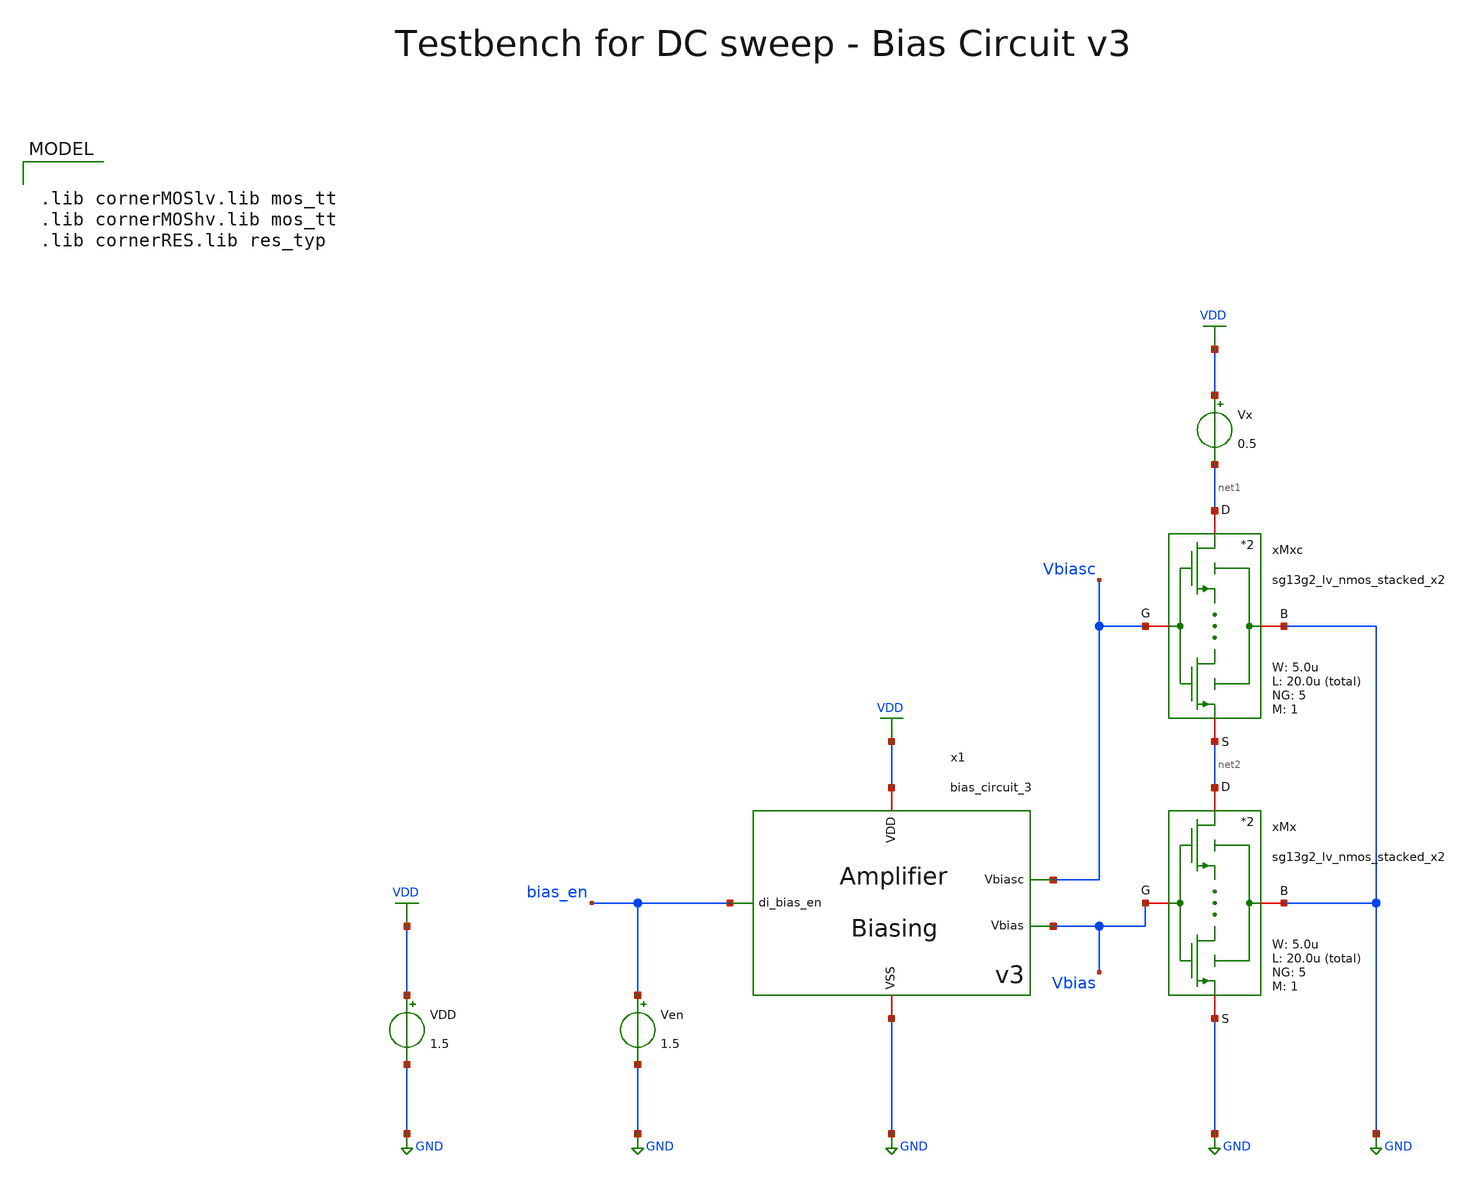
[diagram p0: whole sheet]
** sch_path: SG13G2_ATBS-ADC-main/xschem/bio_amplifier/amplifier_core/bias_circuit/bias_circuit_3/testbenches/bias_circuit_3_tb_dc.sch
**.subckt bias_circuit_3_tb_dc
Ven bias_en GND 1.5
VDD VDD GND 1.5
x1 bias_en VDD GND Vbias Vbiasc bias_circuit_3
Vx VDD net1 0.5
xMx net2 Vbias GND GND sg13g2_lv_nmos_stacked_x2 W_N=5.0u L_N=20.0u NG_N=5 M_N=1
xMxc net1 Vbiasc GND net2 sg13g2_lv_nmos_stacked_x2 W_N=5.0u L_N=20.0u NG_N=5 M_N=1
**** begin user architecture code

.lib cornerMOSlv.lib mos_tt
.lib cornerMOShv.lib mos_tt
.lib cornerRES.lib res_typ



.param temp=27
.options savecurrents method=gear reltol=1e-2 abstol=1e-15 gmin=1e-15
.control

save all

* Operating Point Analysis
op
remzerovec
write bias_circuit_3_tb_dc.raw
set appendwrite

* DC Sweep of Vout
dc Vx 0 1.5 5m
remzerovec
write bias_circuit_3_tb_dc.raw

* Plotting
plot i(Vx) xlabel Vx

* Measurements
meas dc Ix_1V FIND i(Vx) at=1
meas dc Ix_0V FIND i(Vx) at=0
let Ix_volt = Ix_0V - Ix_1V
print Ix_volt

* DC Sweep of VDD
dc VDD 0 1.5 5m
remzerovec
write bias_circuit_3_tb_dc.raw

* Plotting
plot v(Vbias) v(Vbiasc) xlabel VDD
plot i(Vx) xlabel VDD
plot i(v.x1.viref) i(v.x1.viout) xlabel VDD

* Measurements
let Iout_nominal = 10e-9
let Iout_99_percent = 0.99 * Iout_nominal
print Iout_99_percent
meas dc VDD_min WHEN i(v.x1.viout)=Iout_99_percent

meas dc Iout_1_5V FIND i(v.x1.viout) at=1.49
meas dc Iout_1_4V FIND i(v.x1.viout) at=1.39
let Iout_volt = (Iout_1_5V - Iout_1_4V) * 10
print Iout_volt

* Write Data
set wr_vecnames
set wr_singlescale
let Ix=i(Vx)
let Iout=i(v.x1.viout)
wrdata /foss/designs/SG13G2_ATBS-ADC-main/python/plot_simulations/data/bias_circuit_3_tb_dc.txt
+ v(Vbiasc) v(Vbias) v(Ix) v(Iout)

*quit
.endc

**** end user architecture code
**.ends

* expanding   symbol:  bio_amplifier/amplifier_core/bias_circuit/bias_circuit_3/bias_circuit_3.sym #
*+ of pins=5
** sym_path: SG13G2_ATBS-ADC-main/xschem/bio_amplifier/amplifier_core/bias_circuit/bias_circuit_3/bias_circuit_3.sym
** sch_path: SG13G2_ATBS-ADC-main/xschem/bio_amplifier/amplifier_core/bias_circuit/bias_circuit_3/bias_circuit_3.sch
.subckt bias_circuit_3 di_bias_en VDD VSS Vbias Vbiasc
*.iopin VDD
*.iopin VSS
*.opin Vbias
*.ipin di_bias_en
*.opin Vbiasc
XMDEC1 net1 Vbias net1 net1 sg13_lv_nmos w=100.0u l=40.0u ng=100 m=1 mm_ok=1
VIref net4 net7 0
.save i(viref)
VIout net6 Vbiasc 0
.save i(viout)
x1 VDD di_bias_en bias_en_n VSS inverter_lv W_P=1.0u L_P=0.13u W_N=1.0u L_N=0.13u
XMPD1 Vgs_m34 di_bias_en net2 net2 sg13_lv_pmos w=1.0u l=0.13u ng=1 m=1 mm_ok=1
XMPD2 net4 bias_en_n Vgs_m34 net2 sg13_lv_pmos w=1.0u l=0.13u ng=1 m=1 mm_ok=1
VIref5 net1 VSS 0
.save i(viref5)
VIdd VDD net2 0
.save i(vidd)
xM1 net5 net5 VSS net3 sg13g2_lv_nmos_stacked_x2 W_N=20.0u L_N=20.0u NG_N=20 M_N=1
xM1c net7 Vbiasc VSS net5 sg13g2_lv_nmos_stacked_x2 W_N=5.0u L_N=20.0u NG_N=5 M_N=1
xM2 Vbias Vbias VSS VSS sg13g2_lv_nmos_stacked_x2 W_N=5.0u L_N=20.0u NG_N=5 M_N=1
xM2c Vbiasc Vbiasc VSS Vbias sg13g2_lv_nmos_stacked_x2 W_N=5.0u L_N=20.0u NG_N=5 M_N=1
XMDEC2 net2 Vgs_m34 net2 net2 sg13_lv_pmos w=25.0u l=40.0u ng=25 m=1 mm_ok=1
xM3 net4 Vgs_m34 net2 net2 sg13g2_lv_pmos_stacked_x4 W_P=20.0u L_P=40.0u NG_P=20 M_P=1
xM4 net6 Vgs_m34 net2 net2 sg13g2_lv_pmos_stacked_x4 W_P=20.0u L_P=40.0u NG_P=20 M_P=1
x4 di_bias_en Vgs_m34 Vbias net5 VDD VSS aux_ota
R1 net3 VSS 3.521Meg m=1
XMPD3 net5 bias_en_n VSS VSS sg13_lv_nmos w=1.0u l=0.13u ng=1 m=1 mm_ok=1
XMPD4 Vbias bias_en_n VSS VSS sg13_lv_nmos w=1.0u l=0.13u ng=1 m=1 mm_ok=1
xMSU2 Vsu net9 VSS VSS sg13g2_lv_nmos_stacked_x4 W_N=1.0u L_N=40.0u NG_N=1 M_N=1
xMSU1 net8 Vsu VSS net9 sg13g2_lv_nmos_stacked_x4 W_N=1.0u L_N=40.0u NG_N=1 M_N=1
Vmeas1 net4 net8 0
.save i(vmeas1)
Vmeas2 Vbias net9 0
.save i(vmeas2)
CSU1 net10 Vsu 30f m=1
XMPD6 Vsu di_bias_en net10 net10 sg13_lv_pmos w=1.0u l=0.13u ng=1 m=1 mm_ok=1
XMPD7 Vsu bias_en_n VSS VSS sg13_lv_nmos w=1.0u l=0.13u ng=1 m=1 mm_ok=1
XMPD5 net10 bias_en_n net2 net2 sg13_lv_pmos w=1.0u l=0.13u ng=1 m=1 mm_ok=1
.ends


* expanding   symbol:  stacked_transistors/sg13g2_lv_nmos_stacked/sg13g2_lv_nmos_stacked_x2.sym # of
*+ pins=4
** sym_path: SG13G2_ATBS-ADC-main/xschem/stacked_transistors/sg13g2_lv_nmos_stacked/sg13g2_lv_nmos_stacked_x2.sym
** sch_path: SG13G2_ATBS-ADC-main/xschem/stacked_transistors/sg13g2_lv_nmos_stacked/sg13g2_lv_nmos_stacked_x2.sch
.subckt sg13g2_lv_nmos_stacked_x2 D G B S  W_N=1.0u L_N=0.45u NG_N=1 M_N=1
*.iopin D
*.iopin S
*.iopin G
*.iopin B
XM1 net1 G S B sg13_lv_nmos w=W_N l=L_N/2 ng=NG_N m=M_N mm_ok=1
XM2 D G net1 B sg13_lv_nmos w=W_N l=L_N/2 ng=NG_N m=M_N mm_ok=1
.ends


* expanding   symbol:  inverter/inverter_lv.sym # of pins=4
** sym_path: SG13G2_ATBS-ADC-main/xschem/inverter/inverter_lv.sym
** sch_path: SG13G2_ATBS-ADC-main/xschem/inverter/inverter_lv.sch
.subckt inverter_lv VDD vin vout VSS  W_P=3.0u L_P=0.13u W_N=1.0u L_N=0.13u
*.ipin vin
*.iopin VDD
*.iopin VSS
*.opin vout
XM1 vout vin VDD VDD sg13_lv_pmos w=W_P l=L_P ng=1 m=1 mm_ok=1
XM2 vout vin VSS VSS sg13_lv_nmos w=W_N l=L_N ng=1 m=1 mm_ok=1
.ends


* expanding   symbol:  stacked_transistors/sg13g2_lv_pmos_stacked/sg13g2_lv_pmos_stacked_x4.sym # of
*+ pins=4
** sym_path: SG13G2_ATBS-ADC-main/xschem/stacked_transistors/sg13g2_lv_pmos_stacked/sg13g2_lv_pmos_stacked_x4.sym
** sch_path: SG13G2_ATBS-ADC-main/xschem/stacked_transistors/sg13g2_lv_pmos_stacked/sg13g2_lv_pmos_stacked_x4.sch
.subckt sg13g2_lv_pmos_stacked_x4 D G B S  W_P=1.0u L_P=0.45u NG_P=1 M_P=1
*.iopin D
*.iopin S
*.iopin G
*.iopin B
XM1 net1 G S B sg13_lv_pmos w=W_P l=L_P/4 ng=NG_P m=M_P mm_ok=1
XM2 net3 G net1 B sg13_lv_pmos w=W_P l=L_P/4 ng=NG_P m=M_P mm_ok=1
XM3 net2 G net3 B sg13_lv_pmos w=W_P l=L_P/4 ng=NG_P m=M_P mm_ok=1
XM4 D G net2 B sg13_lv_pmos w=W_P l=L_P/4 ng=NG_P m=M_P mm_ok=1
.ends


* expanding   symbol:  bio_amplifier/amplifier_core/bias_circuit/aux_ota/aux_ota.sym # of pins=6
** sym_path: SG13G2_ATBS-ADC-main/xschem/bio_amplifier/amplifier_core/bias_circuit/aux_ota/aux_ota.sym
** sch_path: SG13G2_ATBS-ADC-main/xschem/bio_amplifier/amplifier_core/bias_circuit/aux_ota/aux_ota.sch
.subckt aux_ota di_ota_en vout vinn vinp VDD VSS
*.iopin VDD
*.iopin VSS
*.ipin di_ota_en
*.ipin vinp
*.ipin vinn
*.opin vout
xM3 net1 Vgs_ma34 net2 net2 sg13g2_lv_pmos_stacked_x4 W_P=20.0u L_P=40.0u NG_P=20 M_P=1
xM4 vout Vgs_ma34 net2 net2 sg13g2_lv_pmos_stacked_x4 W_P=20.0u L_P=40.0u NG_P=20 M_P=1
xM1 net1 vinp VSS VSS sg13g2_lv_nmos_stacked_x2 W_N=5.0u L_N=40.0u NG_N=5 M_N=1
VIdd VDD net2 0
.save i(vidd)
xM2 vout vinn VSS VSS sg13g2_lv_nmos_stacked_x2 W_N=5.0u L_N=40.0u NG_N=5 M_N=1
XMPD1 Vgs_ma34 di_ota_en net2 net2 sg13_lv_pmos w=1.0u l=0.13u ng=1 m=1 mm_ok=1
XMPD2 net1 ota_en_n Vgs_ma34 net2 sg13_lv_pmos w=1.0u l=0.13u ng=1 m=1 mm_ok=1
x1 VDD di_ota_en ota_en_n VSS inverter_lv W_P=1.0u L_P=0.13u W_N=1.0u L_N=0.13u
.ends


* expanding   symbol:  stacked_transistors/sg13g2_lv_nmos_stacked/sg13g2_lv_nmos_stacked_x4.sym # of
*+ pins=4
** sym_path: SG13G2_ATBS-ADC-main/xschem/stacked_transistors/sg13g2_lv_nmos_stacked/sg13g2_lv_nmos_stacked_x4.sym
** sch_path: SG13G2_ATBS-ADC-main/xschem/stacked_transistors/sg13g2_lv_nmos_stacked/sg13g2_lv_nmos_stacked_x4.sch
.subckt sg13g2_lv_nmos_stacked_x4 D G B S  W_N=1.0u L_N=0.45u NG_N=1 M_N=1
*.iopin D
*.iopin S
*.iopin G
*.iopin B
XM1 net1 G S B sg13_lv_nmos w=W_N l=L_N/4 ng=NG_N m=M_N mm_ok=1
XM2 net3 G net1 B sg13_lv_nmos w=W_N l=L_N/4 ng=NG_N m=M_N mm_ok=1
XM3 net2 G net3 B sg13_lv_nmos w=W_N l=L_N/4 ng=NG_N m=M_N mm_ok=1
XM4 D G net2 B sg13_lv_nmos w=W_N l=L_N/4 ng=NG_N m=M_N mm_ok=1
.ends

.GLOBAL GND
.GLOBAL VDD
.end
